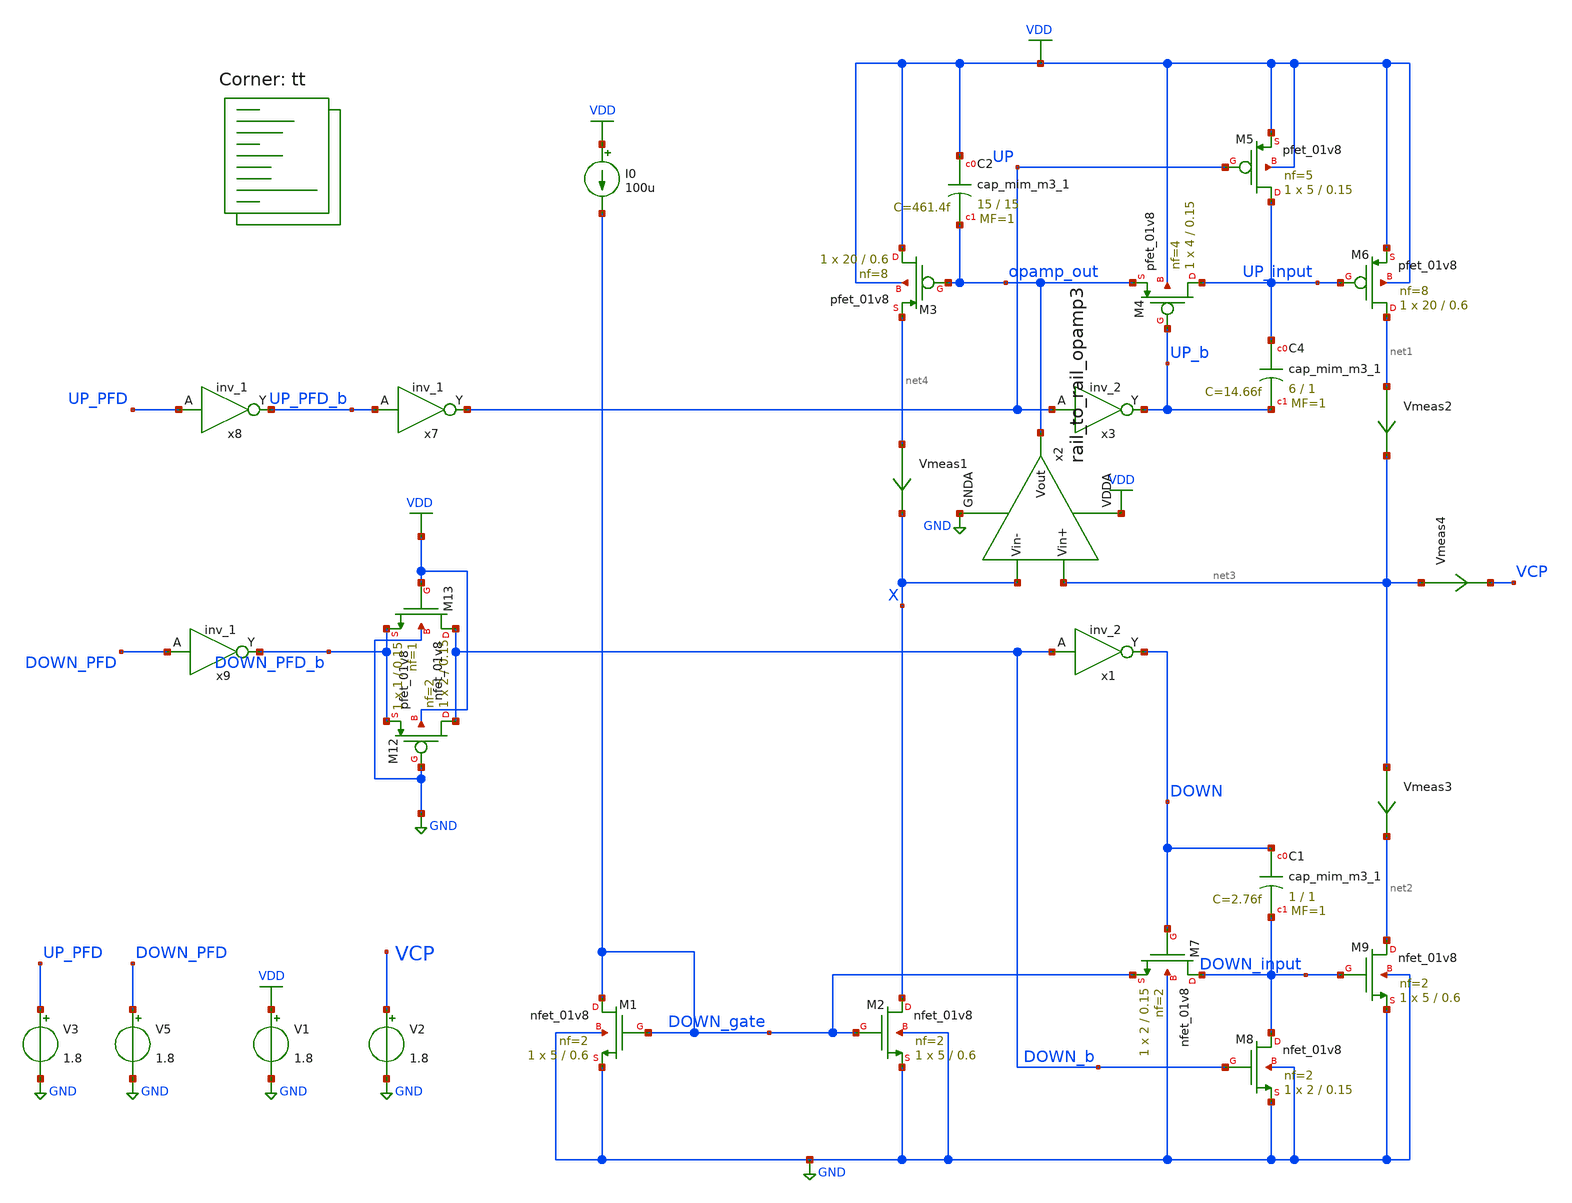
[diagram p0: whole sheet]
** sch_path: projects/pll/charge_pump/xschem_ngspice/charge_pump_DC2.sch
**.subckt charge_pump_DC2
XM1 DOWN_gate DOWN_gate GND GND sky130_fd_pr__nfet_01v8 L=0.6 W=5 nf=2 ad='int((nf+1)/2) * W/nf * 0.29'
+ as='int((nf+2)/2) * W/nf * 0.29' pd='2*int((nf+1)/2) * (W/nf + 0.29)' ps='2*int((nf+2)/2) * (W/nf + 0.29)'
+ nrd='0.29 / W' nrs='0.29 / W' sa=0 sb=0 sd=0 mult=1 m=1
XM2 X DOWN_gate GND GND sky130_fd_pr__nfet_01v8 L=0.6 W=5 nf=2 ad='int((nf+1)/2) * W/nf * 0.29' as='int((nf+2)/2) * W/nf * 0.29'
+ pd='2*int((nf+1)/2) * (W/nf + 0.29)' ps='2*int((nf+2)/2) * (W/nf + 0.29)' nrd='0.29 / W' nrs='0.29 / W'
+ sa=0 sb=0 sd=0 mult=1 m=1
XM3 VDD opamp_out net4 VDD sky130_fd_pr__pfet_01v8 L=0.6 W=20 nf=8 ad='int((nf+1)/2) * W/nf * 0.29' as='int((nf+2)/2) * W/nf * 0.29'
+ pd='2*int((nf+1)/2) * (W/nf + 0.29)' ps='2*int((nf+2)/2) * (W/nf + 0.29)' nrd='0.29 / W' nrs='0.29 / W'
+ sa=0 sb=0 sd=0 mult=1 m=1
V1 VDD GND 1.8
I0 VDD DOWN_gate 100u
Vmeas1 net4 X 0
.save i(vmeas1)
XM4 UP_input UP_b opamp_out VDD sky130_fd_pr__pfet_01v8 L=0.15 W=4 nf=4 ad='int((nf+1)/2) * W/nf * 0.29'
+ as='int((nf+2)/2) * W/nf * 0.29' pd='2*int((nf+1)/2) * (W/nf + 0.29)' ps='2*int((nf+2)/2) * (W/nf + 0.29)'
+ nrd='0.29 / W' nrs='0.29 / W' sa=0 sb=0 sd=0 mult=1 m=1
XM5 UP_input UP VDD VDD sky130_fd_pr__pfet_01v8 L=0.15 W=5 nf=5 ad='int((nf+1)/2) * W/nf * 0.29' as='int((nf+2)/2) * W/nf * 0.29'
+ pd='2*int((nf+1)/2) * (W/nf + 0.29)' ps='2*int((nf+2)/2) * (W/nf + 0.29)' nrd='0.29 / W' nrs='0.29 / W'
+ sa=0 sb=0 sd=0 mult=1 m=1
XM6 net1 UP_input VDD VDD sky130_fd_pr__pfet_01v8 L=0.6 W=20 nf=8 ad='int((nf+1)/2) * W/nf * 0.29' as='int((nf+2)/2) * W/nf * 0.29'
+ pd='2*int((nf+1)/2) * (W/nf + 0.29)' ps='2*int((nf+2)/2) * (W/nf + 0.29)' nrd='0.29 / W' nrs='0.29 / W'
+ sa=0 sb=0 sd=0 mult=1 m=1
Vmeas2 net1 net3 0
.save i(vmeas2)
XM7 DOWN_input DOWN DOWN_gate GND sky130_fd_pr__nfet_01v8 L=0.15 W=2 nf=2 ad='int((nf+1)/2) * W/nf * 0.29'
+ as='int((nf+2)/2) * W/nf * 0.29' pd='2*int((nf+1)/2) * (W/nf + 0.29)' ps='2*int((nf+2)/2) * (W/nf + 0.29)'
+ nrd='0.29 / W' nrs='0.29 / W' sa=0 sb=0 sd=0 mult=1 m=1
XM8 DOWN_input DOWN_b GND GND sky130_fd_pr__nfet_01v8 L=0.15 W=2 nf=2 ad='int((nf+1)/2) * W/nf * 0.29'
+ as='int((nf+2)/2) * W/nf * 0.29' pd='2*int((nf+1)/2) * (W/nf + 0.29)' ps='2*int((nf+2)/2) * (W/nf + 0.29)'
+ nrd='0.29 / W' nrs='0.29 / W' sa=0 sb=0 sd=0 mult=1 m=1
Vmeas3 net3 net2 0
.save i(vmeas3)
XM9 net2 DOWN_input GND GND sky130_fd_pr__nfet_01v8 L=0.6 W=5 nf=2 ad='int((nf+1)/2) * W/nf * 0.29' as='int((nf+2)/2) * W/nf * 0.29'
+ pd='2*int((nf+1)/2) * (W/nf + 0.29)' ps='2*int((nf+2)/2) * (W/nf + 0.29)' nrd='0.29 / W' nrs='0.29 / W'
+ sa=0 sb=0 sd=0 mult=1 m=1
XM12 DOWN_b GND DOWN_PFD_b VDD sky130_fd_pr__pfet_01v8 L=0.15 W=2 nf=2 ad='int((nf+1)/2) * W/nf * 0.29'
+ as='int((nf+2)/2) * W/nf * 0.29' pd='2*int((nf+1)/2) * (W/nf + 0.29)' ps='2*int((nf+2)/2) * (W/nf + 0.29)'
+ nrd='0.29 / W' nrs='0.29 / W' sa=0 sb=0 sd=0 mult=1 m=1
XM13 DOWN_b VDD DOWN_PFD_b GND sky130_fd_pr__nfet_01v8 L=0.15 W=1 nf=1 ad='int((nf+1)/2) * W/nf * 0.29'
+ as='int((nf+2)/2) * W/nf * 0.29' pd='2*int((nf+1)/2) * (W/nf + 0.29)' ps='2*int((nf+2)/2) * (W/nf + 0.29)'
+ nrd='0.29 / W' nrs='0.29 / W' sa=0 sb=0 sd=0 mult=1 m=1
x7 UP_PFD_b GND GND VDD VDD UP sky130_fd_sc_hd__inv_1
x8 UP_PFD GND GND VDD VDD UP_PFD_b sky130_fd_sc_hd__inv_1
x9 DOWN_PFD GND GND VDD VDD DOWN_PFD_b sky130_fd_sc_hd__inv_1
x3 UP GND GND VDD VDD UP_b sky130_fd_sc_hd__inv_2
x1 DOWN_b GND GND VDD VDD DOWN sky130_fd_sc_hd__inv_2
V3 UP_PFD GND 1.8
V5 DOWN_PFD GND 1.8
x2 VDD net3 X opamp_out GND rail_to_rail_opamp3
V2 VCP GND 1.8
Vmeas4 net3 VCP 0
.save i(vmeas4)
XC4 UP_input UP_b sky130_fd_pr__cap_mim_m3_1 W=6 L=1 MF=1 m=1
XC1 DOWN DOWN_input sky130_fd_pr__cap_mim_m3_1 W=1 L=1 MF=1 m=1
XC2 VDD opamp_out sky130_fd_pr__cap_mim_m3_1 W=15 L=15 MF=1 m=1
**** begin user architecture code
.lib $::SKYWATER_MODELS/sky130.lib.spice tt



.include /foss/pdks/sky130A/libs.ref/sky130_fd_sc_hd/spice/sky130_fd_sc_hd.spice

.option method=gear trtol1
.option wnflag=1
.option savecurrents

* .temp = 75

* .ic v(vout) = 0

.save  v(up_pfd) v(down_pfd) v(up_pfd_b) v(down_pfd_b) v(up) v(up_b) v(down) v(down_b) v(v2) v(x) v(vcp) v(up_input) v(down_input) v(down_gate) v(opamp_out) v(x2.p_bias) v(x2.n_bias) v(x2.v_common_p) v(x2.v_common_n) v(x2.p_left) v(x2.p_right) v(x2.n_left) v(x2.n_right) v(f_ref) v(f_vco) v(x4.qa) v(x4.qa_b) v(x4.qb) v(x4.qb_b) v(x4.qa) v(x4.e) v(x4.e_b) v(x4.f) v(x4.f_b) v(x4.before_reset) v(x4.reset)


.control
  * save v(up_pfd) v(down_pfd) v(up_pfd_b) v(down_pfd_b) v(up) v(up_b) v(down) v(down_b) v(x)
+ v(vout) v(up_input) v(down_input)
  * save all

  * tran 1ns 10us
  dc v2 0 1.8 0.01 v3 0 1.8 1.8
  remzerovec
  write charge_pump_DC2.raw
  * wrdata /foss/designs/my_design/projects/pll/pfd/xschem_ngspice/charge_pump2_QA.txt v(osc)
  set appendwrite

.endc






**** end user architecture code
**.ends

* expanding   symbol:
*+  /foss/designs/my_design/projects/pll/charge_pump/xschem_ngspice/rail_to_rail_opamp3.sym # of pins=5
** sym_path: projects/pll/charge_pump/xschem_ngspice/rail_to_rail_opamp3.sym
** sch_path: projects/pll/charge_pump/xschem_ngspice/rail_to_rail_opamp3.sch
.subckt rail_to_rail_opamp3 VDDA Vin+ Vin- Vout GNDA
*.opin Vout
*.ipin Vin+
*.ipin Vin-
*.ipin VDDA
*.ipin GNDA
XM2 n_left Vin+ v_common_n GNDA sky130_fd_pr__nfet_01v8 L=0.15 W=1 nf=1 ad='int((nf+1)/2) * W/nf * 0.29'
+ as='int((nf+2)/2) * W/nf * 0.29' pd='2*int((nf+1)/2) * (W/nf + 0.29)' ps='2*int((nf+2)/2) * (W/nf + 0.29)'
+ nrd='0.29 / W' nrs='0.29 / W' sa=0 sb=0 sd=0 mult=1 m=1
XM3 n_right Vin- v_common_n GNDA sky130_fd_pr__nfet_01v8 L=0.15 W=1 nf=1 ad='int((nf+1)/2) * W/nf * 0.29'
+ as='int((nf+2)/2) * W/nf * 0.29' pd='2*int((nf+1)/2) * (W/nf + 0.29)' ps='2*int((nf+2)/2) * (W/nf + 0.29)'
+ nrd='0.29 / W' nrs='0.29 / W' sa=0 sb=0 sd=0 mult=1 m=1
XM5 n_left n_left VDDA VDDA sky130_fd_pr__pfet_01v8 L=0.15 W=2 nf=2 ad='int((nf+1)/2) * W/nf * 0.29'
+ as='int((nf+2)/2) * W/nf * 0.29' pd='2*int((nf+1)/2) * (W/nf + 0.29)' ps='2*int((nf+2)/2) * (W/nf + 0.29)'
+ nrd='0.29 / W' nrs='0.29 / W' sa=0 sb=0 sd=0 mult=1 m=1
XM4 n_right n_left VDDA VDDA sky130_fd_pr__pfet_01v8 L=0.15 W=2 nf=2 ad='int((nf+1)/2) * W/nf * 0.29'
+ as='int((nf+2)/2) * W/nf * 0.29' pd='2*int((nf+1)/2) * (W/nf + 0.29)' ps='2*int((nf+2)/2) * (W/nf + 0.29)'
+ nrd='0.29 / W' nrs='0.29 / W' sa=0 sb=0 sd=0 mult=1 m=1
XM6 v_common_p p_bias VDDA VDDA sky130_fd_pr__pfet_01v8 L=0.15 W=3 nf=3 ad='int((nf+1)/2) * W/nf * 0.29'
+ as='int((nf+2)/2) * W/nf * 0.29' pd='2*int((nf+1)/2) * (W/nf + 0.29)' ps='2*int((nf+2)/2) * (W/nf + 0.29)'
+ nrd='0.29 / W' nrs='0.29 / W' sa=0 sb=0 sd=0 mult=1 m=1
XM7 p_left Vin+ v_common_p VDDA sky130_fd_pr__pfet_01v8 L=0.15 W=2 nf=2 ad='int((nf+1)/2) * W/nf * 0.29'
+ as='int((nf+2)/2) * W/nf * 0.29' pd='2*int((nf+1)/2) * (W/nf + 0.29)' ps='2*int((nf+2)/2) * (W/nf + 0.29)'
+ nrd='0.29 / W' nrs='0.29 / W' sa=0 sb=0 sd=0 mult=1 m=1
XM8 p_right Vin- v_common_p VDDA sky130_fd_pr__pfet_01v8 L=0.15 W=2 nf=2 ad='int((nf+1)/2) * W/nf * 0.29'
+ as='int((nf+2)/2) * W/nf * 0.29' pd='2*int((nf+1)/2) * (W/nf + 0.29)' ps='2*int((nf+2)/2) * (W/nf + 0.29)'
+ nrd='0.29 / W' nrs='0.29 / W' sa=0 sb=0 sd=0 mult=1 m=1
XM9 p_left p_left GNDA GNDA sky130_fd_pr__nfet_01v8 L=0.15 W=1 nf=1 ad='int((nf+1)/2) * W/nf * 0.29'
+ as='int((nf+2)/2) * W/nf * 0.29' pd='2*int((nf+1)/2) * (W/nf + 0.29)' ps='2*int((nf+2)/2) * (W/nf + 0.29)'
+ nrd='0.29 / W' nrs='0.29 / W' sa=0 sb=0 sd=0 mult=1 m=1
XM10 p_right p_left GNDA GNDA sky130_fd_pr__nfet_01v8 L=0.15 W=1 nf=1 ad='int((nf+1)/2) * W/nf * 0.29'
+ as='int((nf+2)/2) * W/nf * 0.29' pd='2*int((nf+1)/2) * (W/nf + 0.29)' ps='2*int((nf+2)/2) * (W/nf + 0.29)'
+ nrd='0.29 / W' nrs='0.29 / W' sa=0 sb=0 sd=0 mult=1 m=1
XM1 v_common_n n_bias GNDA GNDA sky130_fd_pr__nfet_01v8 L=0.15 W=1 nf=1 ad='int((nf+1)/2) * W/nf * 0.29'
+ as='int((nf+2)/2) * W/nf * 0.29' pd='2*int((nf+1)/2) * (W/nf + 0.29)' ps='2*int((nf+2)/2) * (W/nf + 0.29)'
+ nrd='0.29 / W' nrs='0.29 / W' sa=0 sb=0 sd=0 mult=1 m=1
XM11 Vout n_right VDDA VDDA sky130_fd_pr__pfet_01v8 L=0.15 W=16 nf=2 ad='int((nf+1)/2) * W/nf * 0.29'
+ as='int((nf+2)/2) * W/nf * 0.29' pd='2*int((nf+1)/2) * (W/nf + 0.29)' ps='2*int((nf+2)/2) * (W/nf + 0.29)'
+ nrd='0.29 / W' nrs='0.29 / W' sa=0 sb=0 sd=0 mult=1 m=1
XM12 Vout p_right GNDA GNDA sky130_fd_pr__nfet_01v8 L=0.15 W=8 nf=1 ad='int((nf+1)/2) * W/nf * 0.29'
+ as='int((nf+2)/2) * W/nf * 0.29' pd='2*int((nf+1)/2) * (W/nf + 0.29)' ps='2*int((nf+2)/2) * (W/nf + 0.29)'
+ nrd='0.29 / W' nrs='0.29 / W' sa=0 sb=0 sd=0 mult=1 m=1
XM13 n_bias n_bias GNDA GNDA sky130_fd_pr__nfet_01v8 L=0.15 W=1 nf=1 ad='int((nf+1)/2) * W/nf * 0.29'
+ as='int((nf+2)/2) * W/nf * 0.29' pd='2*int((nf+1)/2) * (W/nf + 0.29)' ps='2*int((nf+2)/2) * (W/nf + 0.29)'
+ nrd='0.29 / W' nrs='0.29 / W' sa=0 sb=0 sd=0 mult=1 m=1
XM15 p_bias p_bias VDDA VDDA sky130_fd_pr__pfet_01v8 L=0.15 W=2 nf=2 ad='int((nf+1)/2) * W/nf * 0.29'
+ as='int((nf+2)/2) * W/nf * 0.29' pd='2*int((nf+1)/2) * (W/nf + 0.29)' ps='2*int((nf+2)/2) * (W/nf + 0.29)'
+ nrd='0.29 / W' nrs='0.29 / W' sa=0 sb=0 sd=0 mult=1 m=1
Vmeas net1 n_bias 0
.save i(vmeas)
XM14 net1 net1 p_bias p_bias sky130_fd_pr__pfet_01v8 L=0.15 W=2 nf=2 ad='int((nf+1)/2) * W/nf * 0.29'
+ as='int((nf+2)/2) * W/nf * 0.29' pd='2*int((nf+1)/2) * (W/nf + 0.29)' ps='2*int((nf+2)/2) * (W/nf + 0.29)'
+ nrd='0.29 / W' nrs='0.29 / W' sa=0 sb=0 sd=0 mult=1 m=1
.ends

.GLOBAL VDD
.GLOBAL GND
.end
